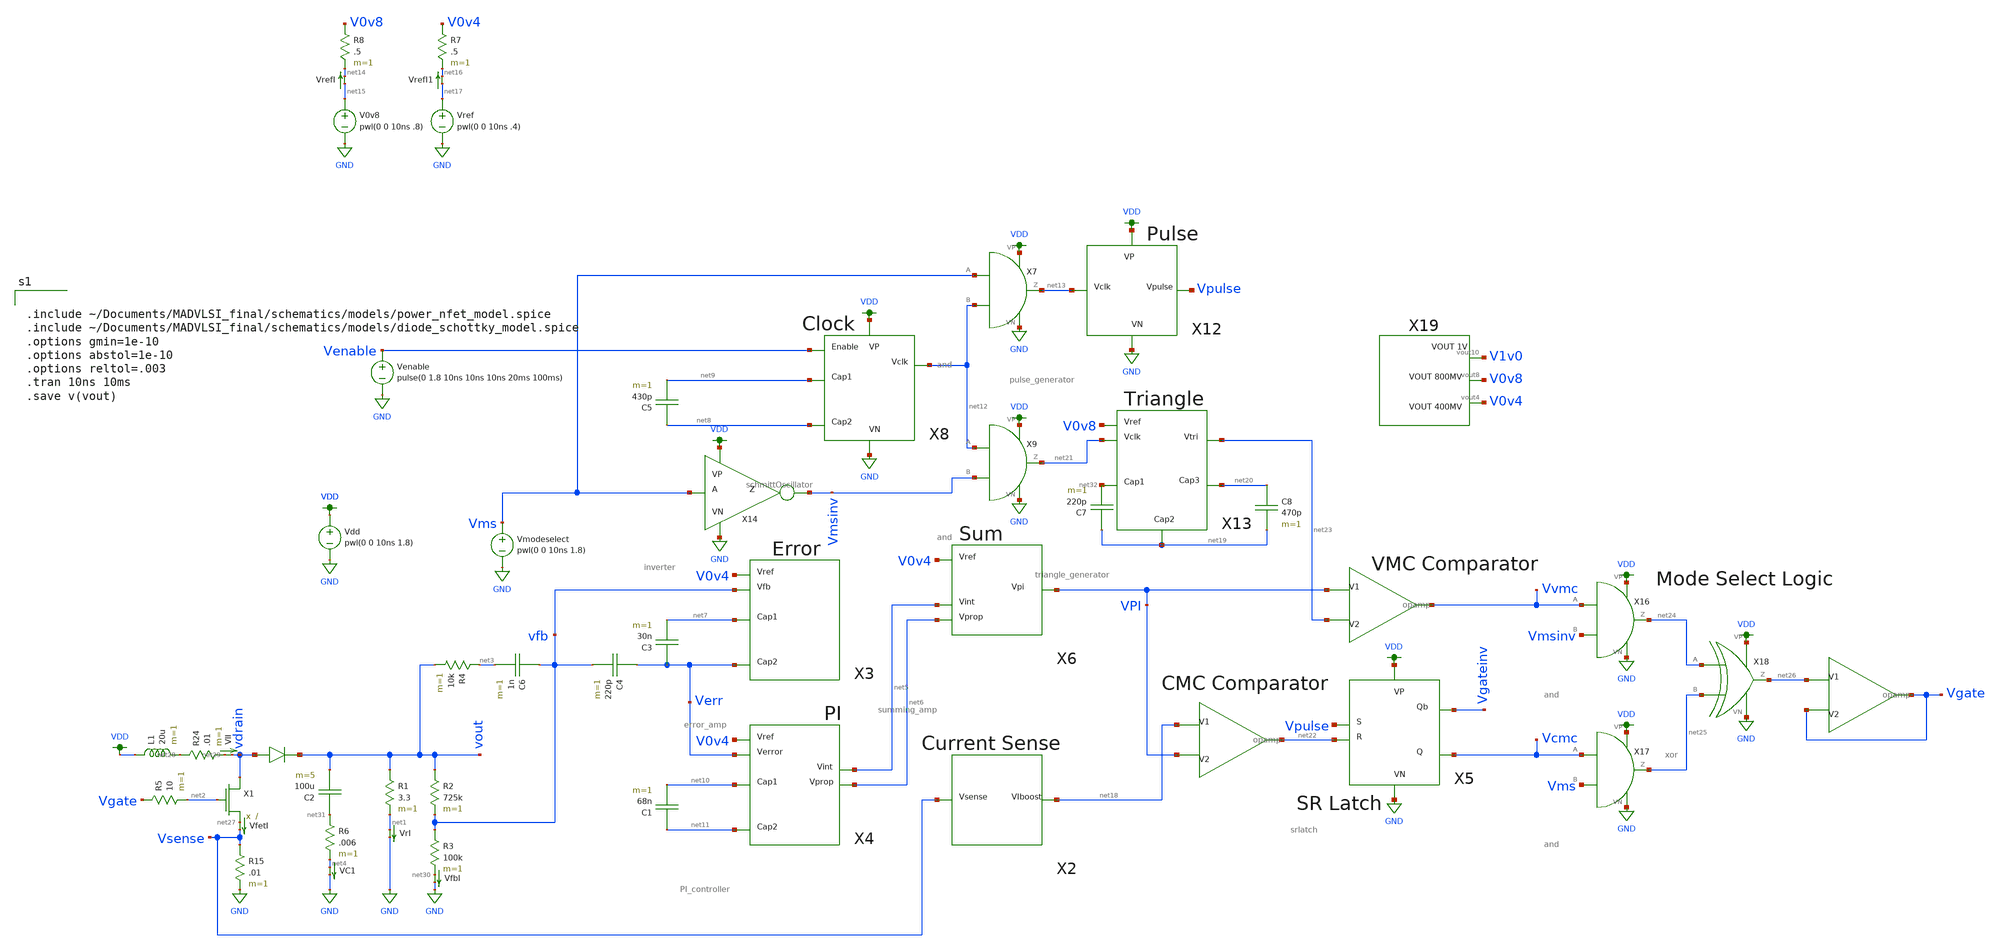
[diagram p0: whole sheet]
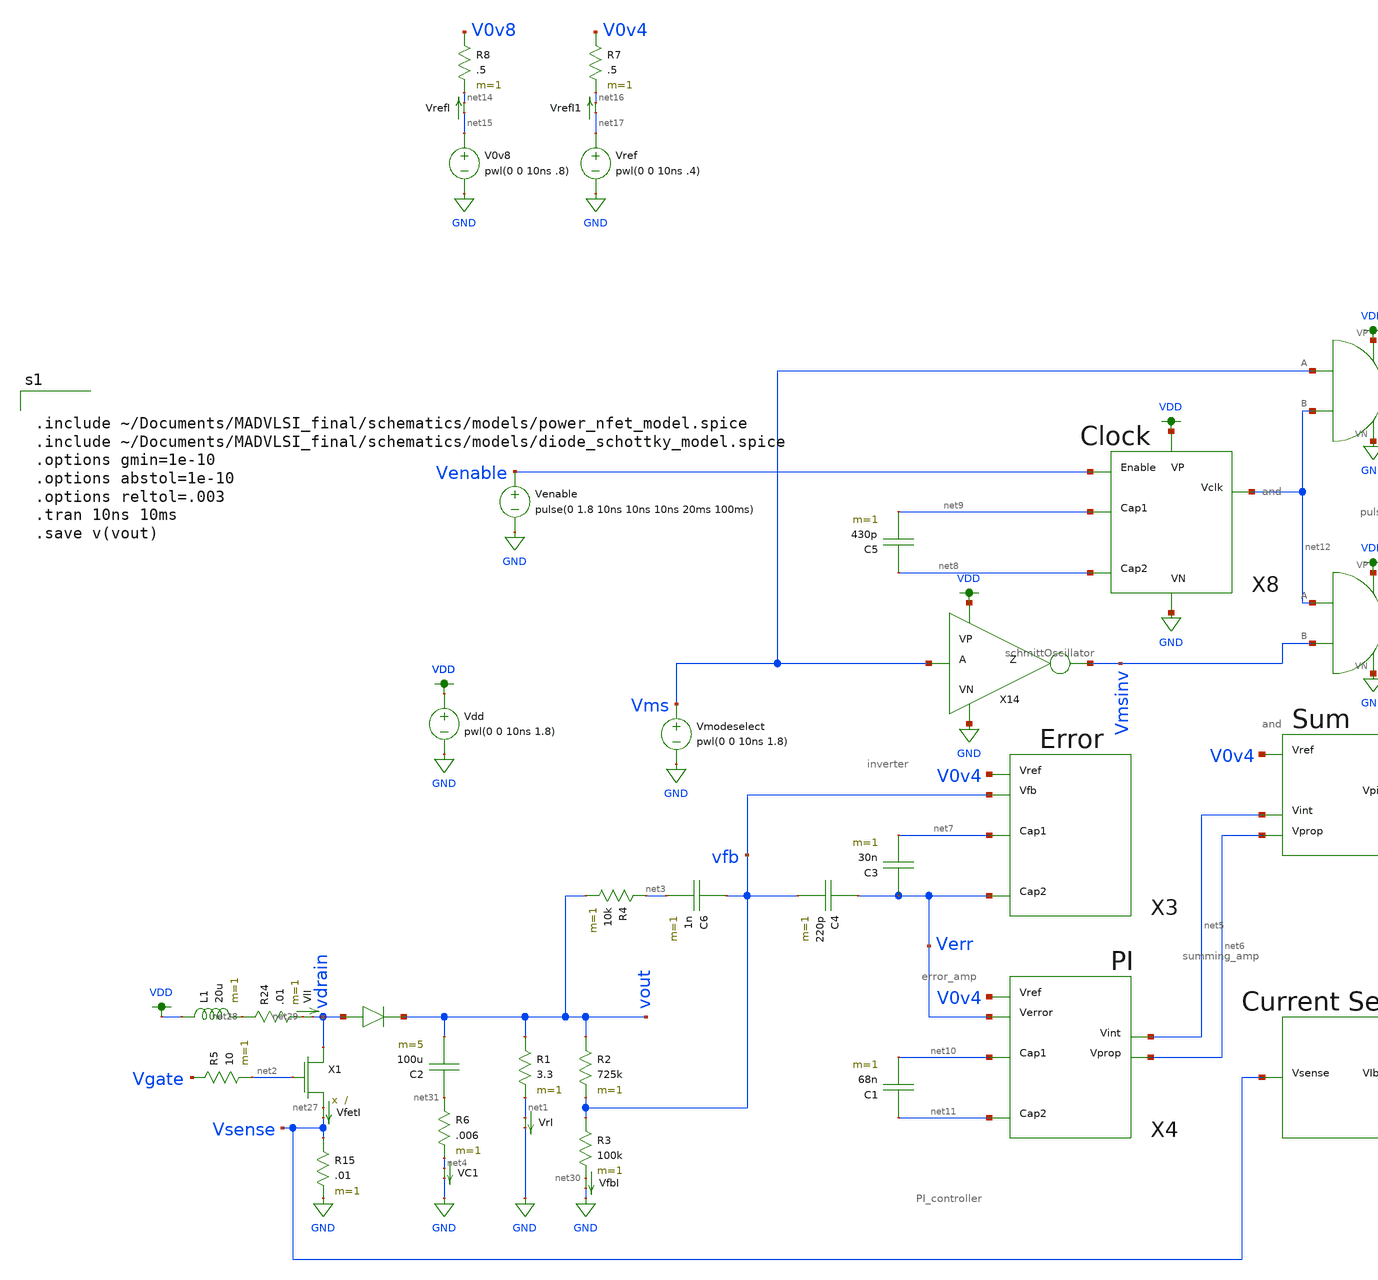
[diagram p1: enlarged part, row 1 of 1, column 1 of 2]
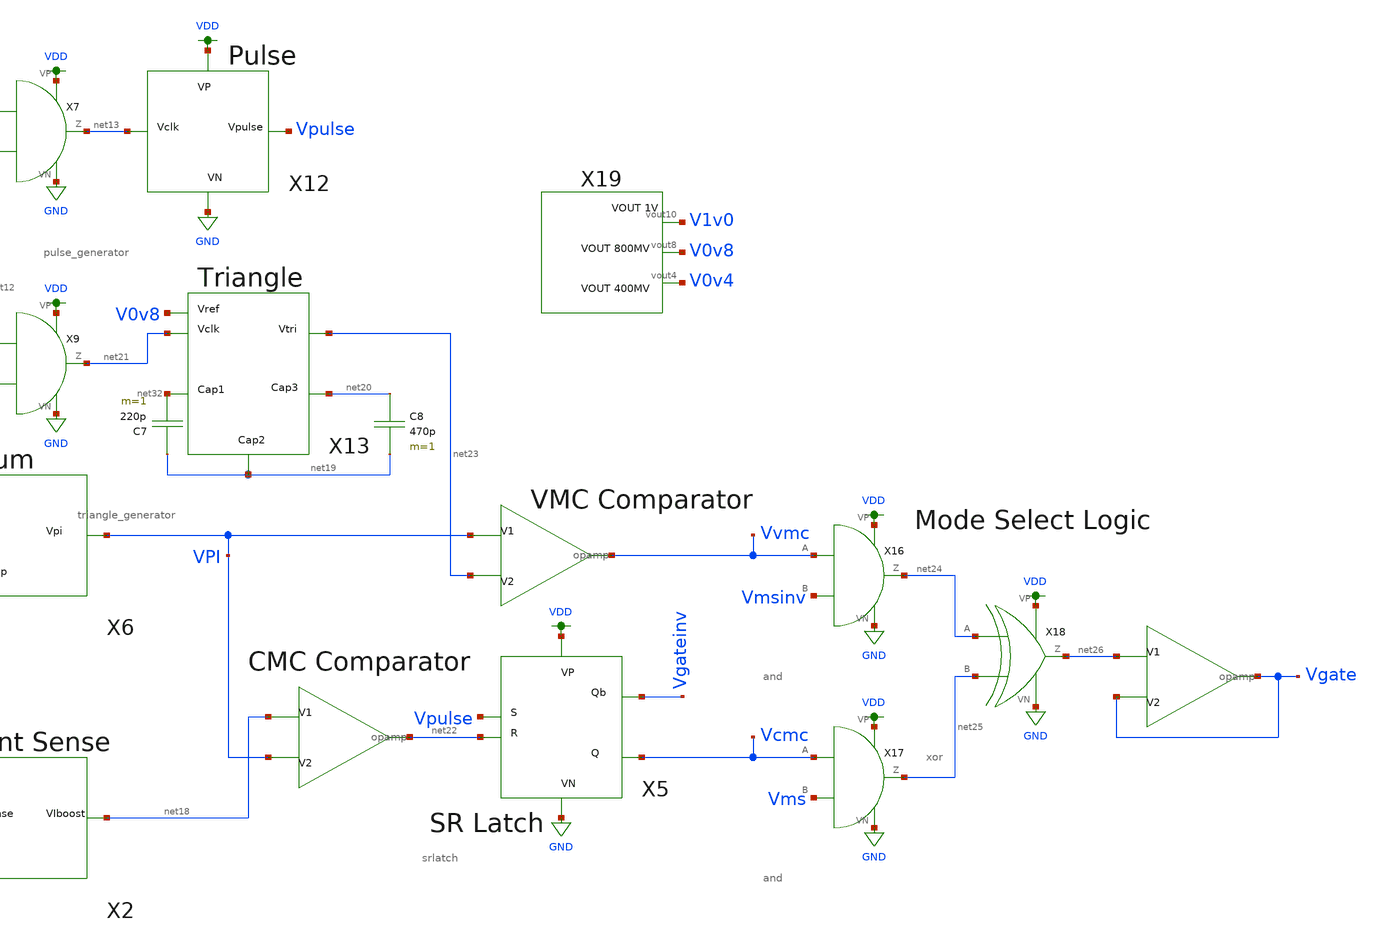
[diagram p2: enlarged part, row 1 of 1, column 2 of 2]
** sch_path: schematics/boost_controller.sch
**.subckt boost_controller
VfetI net27 Vsense 0
.save i(vfeti)
X1 vdrain net2 net27 power_nfet
L1 VDD net28 20u m=1
D1 vdrain vout diode_schottky
R1 vout net1 3.3 m=1
VlI net29 vdrain 0
.save i(vli)
VrI net1 GND 0
.save i(vri)
R2 vout vfb 725k m=1
R3 vfb net30 100k m=1
Vdd VDD GND pwl(0 0 10ns 1.8)
Vref net17 GND pwl(0 0 10ns .4)
X11 net18 VPI net22 opamp
R24 net28 net29 .01 m=1
VfbI net30 GND 0
.save i(vfbi)
C3 Verr net7 30n m=1
C4 Verr vfb 220p m=1
R4 net3 vout 10k m=1
C6 vfb net3 1n m=1
R5 Vgate net2 10 m=1
C2 net31 vout 100u m=5
R6 net31 net4 .006 m=1
VC1 net4 GND 0
.save i(vc1)
R15 Vsense GND .01 m=1
X5 Vpulse net22 VDD GND Vgateinv Vcmc srlatch
X10 net26 Vgate Vgate opamp
Venable Venable GND pulse(0 1.8 10ns 10ns 10ns 20ms 100ms)
X2 Vsense net18 current_boost
X3 V0v4 net7 vfb Verr error_amp
X4 V0v4 net10 Verr net11 net5 net6 PI_controller
C1 net11 net10 68n m=1
X6 V0v4 VPI net5 net6 summing_amp
X8 Venable net9 net8 VDD GND net12 schmittOscillator
C5 net8 net9 430p m=1
X12 Vpulse VDD GND net13 pulse_generator
X7 Vms net12 VDD GND net13 and
X9 net12 Vmsinv VDD GND net21 and
Vmodeselect Vms GND pwl(0 0 10ns 1.8)
X13 net23 V0v8 net32 net21 net19 net20 triangle_generator
X14 Vms VDD GND Vmsinv inverter
V0v8 net15 GND pwl(0 0 10ns .8)
VrefI net15 net14 0
.save i(vrefi)
R8 V0v8 net14 .5 m=1
VrefI1 net17 net16 0
.save i(vrefi1)
R7 V0v4 net16 .5 m=1
X15 VPI net23 Vvmc opamp
C7 net19 net32 220p m=1
C8 net20 net19 470p m=1
X16 Vvmc Vmsinv VDD GND net24 and
X17 Vcmc Vms VDD GND net25 and
X18 net24 net25 VDD GND net26 xor
X19 V0v8 V1v0 V0v4 bandgap_LDS
**** begin user architecture code


.include ~/Documents/MADVLSI_final/schematics/models/power_nfet_model.spice
.include ~/Documents/MADVLSI_final/schematics/models/diode_schottky_model.spice
.options gmin=1e-10
.options abstol=1e-10
.options reltol=.003
.tran 10ns 10ms
.save v(vout)


.option wnflag=1
.lib ~/skywater/skywater-pdk/libraries/sky130_fd_pr_ngspice/latest/models/sky130.lib.spice tt

**** end user architecture code
**.ends
.GLOBAL GND
.GLOBAL VDD
.end
